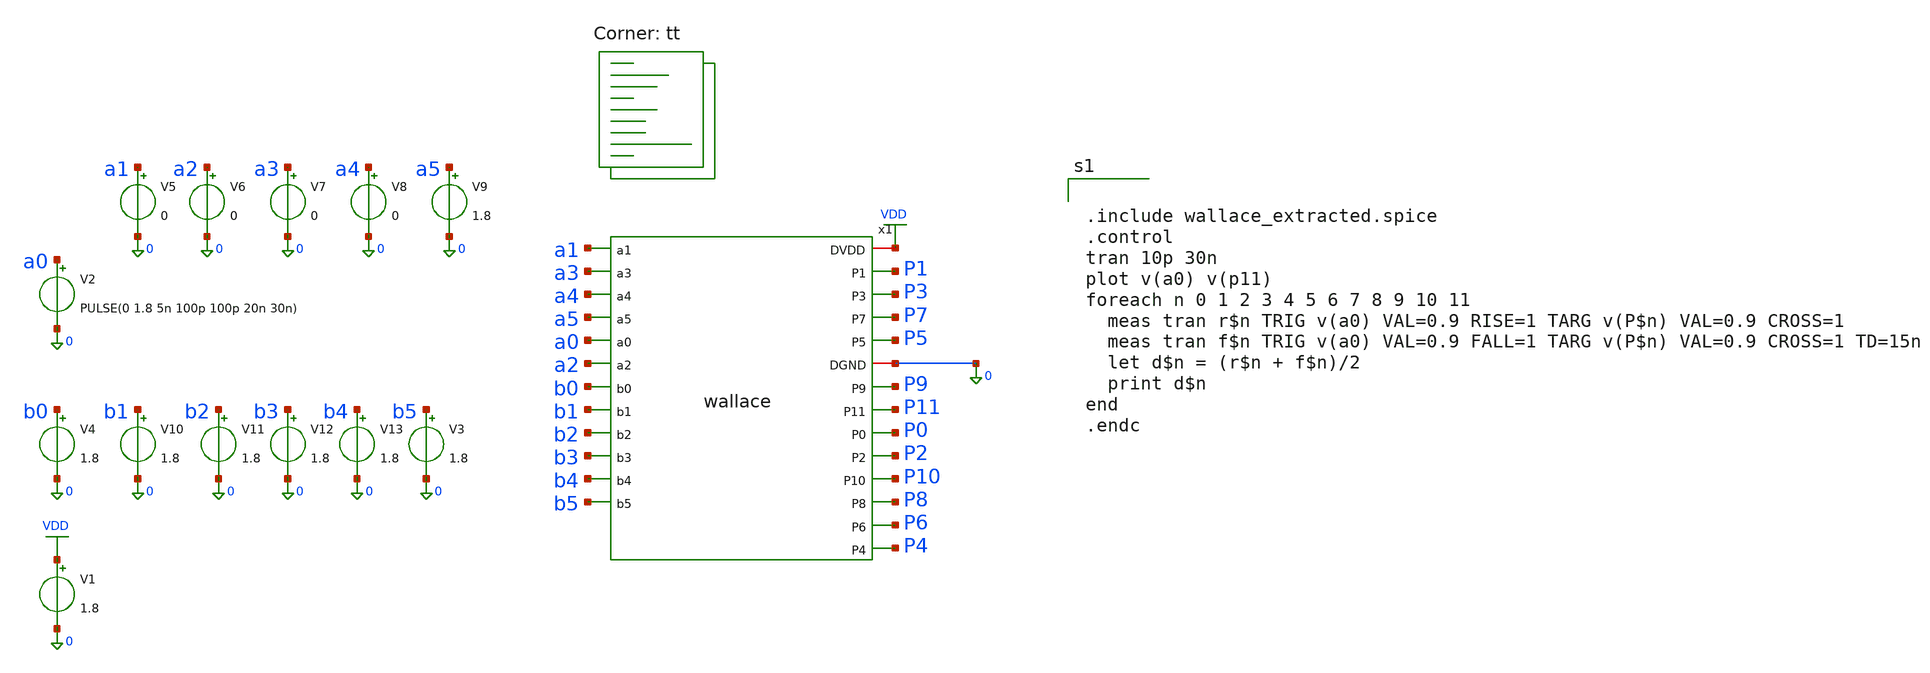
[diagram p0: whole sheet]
** sch_path: xschem/post_layout.sch
**.subckt post_layout
V1 VDD 0 1.8
V3 b5 0 1.8
V4 b0 0 1.8
V2 a0 0 PULSE(0 1.8 5n 100p 100p 20n 30n)
V5 a1 0 0
V6 a2 0 0
V7 a3 0 0
V8 a4 0 0
V9 a5 0 1.8
V10 b1 0 1.8
V11 b2 0 1.8
V12 b3 0 1.8
V13 b4 0 1.8
x1 VDD a1 P1 a3 P3 P7 a4 P5 a5 a0 a2 b0 b1 b2 b3 0 b4 b5 P9 P11 P0 P2 P10 P8 P6 P4 wallace
**** begin user architecture code


.include wallace_extracted.spice
.control
tran 10p 30n
plot v(a0) v(p11)
foreach n 0 1 2 3 4 5 6 7 8 9 10 11
  meas tran r$n TRIG v(a0) VAL=0.9 RISE=1 TARG v(P$n) VAL=0.9 CROSS=1
  meas tran f$n TRIG v(a0) VAL=0.9 FALL=1 TARG v(P$n) VAL=0.9 CROSS=1 TD=15n
  let d$n = (r$n + f$n)/2
  print d$n
end
.endc

.lib $::SKYWATER_MODELS/sky130.lib.spice tt
**** end user architecture code
**.ends
.GLOBAL VDD
.end
